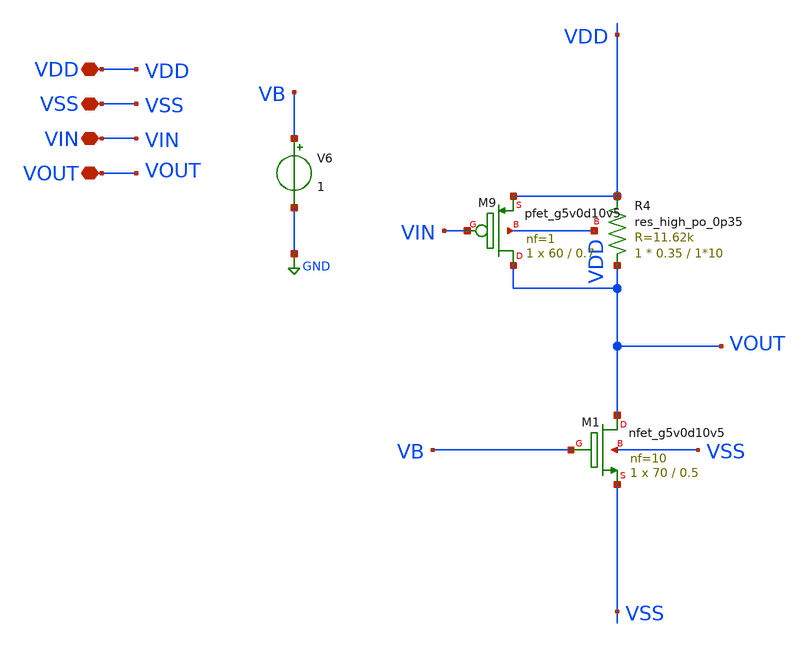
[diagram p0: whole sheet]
** sch_path: old stuff/amplifiers/single_stage_amps/stange_stages/source_follower_2/source_follower_2_stage.sch
**.subckt source_follower_2_stage VDD VSS VIN VOUT
*.iopin VDD
*.iopin VSS
*.iopin VIN
*.iopin VOUT
XM1 VOUT VB VSS VSS sky130_fd_pr__nfet_g5v0d10v5 L=0.5 W=70 nf=10 ad='int((nf+1)/2) * W/nf * 0.29' as='int((nf+2)/2) * W/nf * 0.29'
+ pd='2*int((nf+1)/2) * (W/nf + 0.29)' ps='2*int((nf+2)/2) * (W/nf + 0.29)' nrd='0.29 / W' nrs='0.29 / W'
+ sa=0 sb=0 sd=0 mult=1 m=1
XR4 VOUT VDD VDD sky130_fd_pr__res_high_po_0p35 L=1*10 mult=1 m=1
XM9 VOUT VIN VDD VDD sky130_fd_pr__pfet_g5v0d10v5 L=0.7 W=60 nf=1 ad='int((1 + 1)/2) * 60 / 1 * 0.29'
+ as='int((1 + 2)/2) * 60 / 1 * 0.29' pd='2*int((1 + 1)/2) * (60 / 1 + 0.29)' ps='2*int((1 + 2)/2) * (60 / 1 + 0.29)'
+ nrd='0.29 / 60 ' nrs='0.29 / 60 ' sa=0 sb=0 sd=0 mult=1 m=1
V6 VB GND 1
**.ends
.GLOBAL GND
.end
